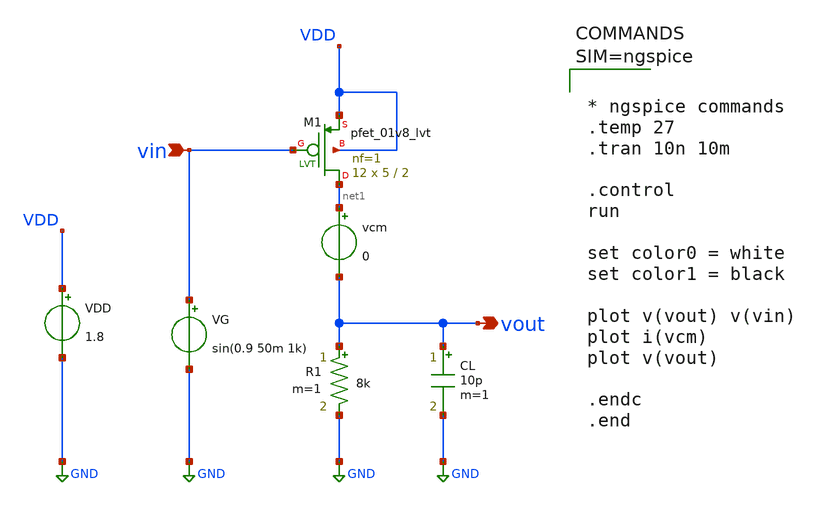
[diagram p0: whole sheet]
** sch_path: Common_Source_PMOS_Restitive_ckts/CS_Amp_PMOS_Restitive_Load_AC_Transient_Analysis.sch
**.subckt CS_Amp_PMOS_Restitive_Load_AC_Transient_Analysis vout vin
*.opin vout
*.ipin vin
R1 vout GND 8k m=1
CL vout GND 10p m=1
VG vin GND sin(0.9 50m 1k)
VDD VDD GND 1.8
vcm net1 vout 0
XM1 net1 vin VDD VDD sky130_fd_pr__pfet_01v8_lvt L=2 W=5 nf=1 ad='int((1 + 1)/2) * 5 / 1 * 0.29' as='int((1 + 2)/2) * 5 / 1 * 0.29'
+ pd='2*int((1 + 1)/2) * (5 / 1 + 0.29)' ps='2*int((1 + 2)/2) * (5 / 1 + 0.29)' nrd='0.29 / 5 ' nrs='0.29 / 5 '
+ sa=0 sb=0 sd=0 mult=12 m=12
**** begin user architecture code



* ngspice commands
.temp 27
.tran 10n 10m

.control
run

set color0 = white
set color1 = black

plot v(vout) v(vin)
plot i(vcm)
plot v(vout)

.endc
.end





** opencircuitdesign pdks install
.lib $::SKYWATER_MODELS/sky130.lib.spice tt

**** end user architecture code
**.ends
.GLOBAL GND
.end
